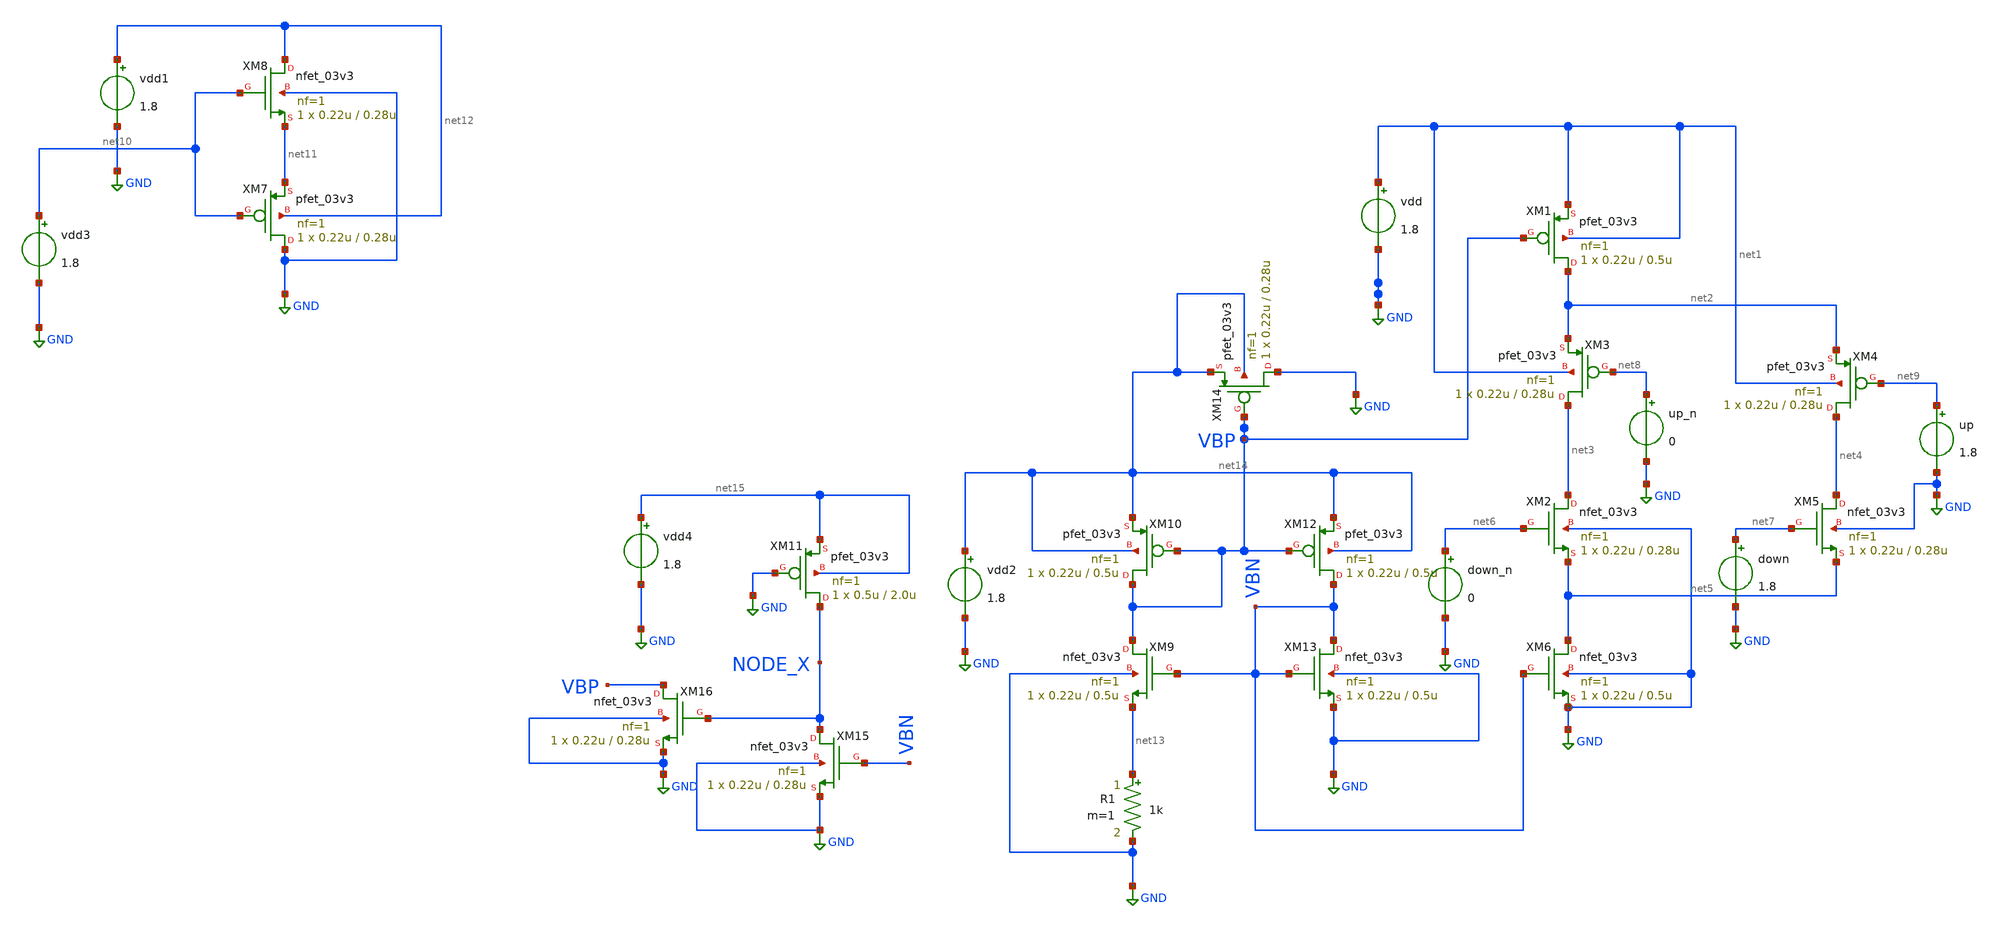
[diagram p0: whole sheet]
** sch_path: src/ChargePump/cp_amp.sch
* Copyright 2022 GlobalFoundries PDK Authors
* Licensed under the Apache License, Version 2.0 (the "License");
* you may not use this file except in compliance with the License.
* You may obtain a copy of the License at
* https://www.apache.org/licenses/LICENSE-2.0
* Unless required by applicable law or agreed to in writing, software
* distributed under the License is distributed on an "AS IS" BASIS,
* WITHOUT WARRANTIES OR CONDITIONS OF ANY KIND, either express or implied.
* See the License for the specific language governing permissions and
* limitations under the License.
**.subckt cp_amp
XM1 net2 VBP net1 net1 pfet_03v3 L=0.5u W=0.22u nf=1 ad='int((nf+1)/2) * W/nf * 0.18u' as='int((nf+2)/2) * W/nf * 0.18u'
+ pd='2*int((nf+1)/2) * (W/nf + 0.18u)' ps='2*int((nf+2)/2) * (W/nf + 0.18u)' nrd='0.18u / W' nrs='0.18u / W'
+ sa=0 sb=0 sd=0 m=1
XM2 net3 net6 net5 GND nfet_03v3 L=0.28u W=0.22u nf=1 ad='int((nf+1)/2) * W/nf * 0.18u' as='int((nf+2)/2) * W/nf * 0.18u'
+ pd='2*int((nf+1)/2) * (W/nf + 0.18u)' ps='2*int((nf+2)/2) * (W/nf + 0.18u)' nrd='0.18u / W' nrs='0.18u / W'
+ sa=0 sb=0 sd=0 m=1
vdd net1 GND 1.8
XM3 net3 net8 net2 net1 pfet_03v3 L=0.28u W=0.22u nf=1 ad='int((nf+1)/2) * W/nf * 0.18u' as='int((nf+2)/2) * W/nf * 0.18u'
+ pd='2*int((nf+1)/2) * (W/nf + 0.18u)' ps='2*int((nf+2)/2) * (W/nf + 0.18u)' nrd='0.18u / W' nrs='0.18u / W'
+ sa=0 sb=0 sd=0 m=1
XM4 net4 net9 net2 net1 pfet_03v3 L=0.28u W=0.22u nf=1 ad='int((nf+1)/2) * W/nf * 0.18u' as='int((nf+2)/2) * W/nf * 0.18u'
+ pd='2*int((nf+1)/2) * (W/nf + 0.18u)' ps='2*int((nf+2)/2) * (W/nf + 0.18u)' nrd='0.18u / W' nrs='0.18u / W'
+ sa=0 sb=0 sd=0 m=1
XM5 net4 net7 net5 GND nfet_03v3 L=0.28u W=0.22u nf=1 ad='int((nf+1)/2) * W/nf * 0.18u' as='int((nf+2)/2) * W/nf * 0.18u'
+ pd='2*int((nf+1)/2) * (W/nf + 0.18u)' ps='2*int((nf+2)/2) * (W/nf + 0.18u)' nrd='0.18u / W' nrs='0.18u / W'
+ sa=0 sb=0 sd=0 m=1
XM6 net5 VBN GND GND nfet_03v3 L=0.5u W=0.22u nf=1 ad='int((nf+1)/2) * W/nf * 0.18u' as='int((nf+2)/2) * W/nf * 0.18u'
+ pd='2*int((nf+1)/2) * (W/nf + 0.18u)' ps='2*int((nf+2)/2) * (W/nf + 0.18u)' nrd='0.18u / W' nrs='0.18u / W'
+ sa=0 sb=0 sd=0 m=1
down net7 GND 1.8
up net9 GND 1.8
up_n net8 GND 0
down_n net6 GND 0
XM7 GND net10 net11 net12 pfet_03v3 L=0.28u W=0.22u nf=1 ad='int((nf+1)/2) * W/nf * 0.18u' as='int((nf+2)/2) * W/nf * 0.18u'
+ pd='2*int((nf+1)/2) * (W/nf + 0.18u)' ps='2*int((nf+2)/2) * (W/nf + 0.18u)' nrd='0.18u / W' nrs='0.18u / W'
+ sa=0 sb=0 sd=0 m=1
XM8 net12 net10 net11 GND nfet_03v3 L=0.28u W=0.22u nf=1 ad='int((nf+1)/2) * W/nf * 0.18u' as='int((nf+2)/2) * W/nf * 0.18u'
+ pd='2*int((nf+1)/2) * (W/nf + 0.18u)' ps='2*int((nf+2)/2) * (W/nf + 0.18u)' nrd='0.18u / W' nrs='0.18u / W'
+ sa=0 sb=0 sd=0 m=1
vdd1 net12 GND 1.8
vdd2 net14 GND 1.8
XM10 VBP VBP net14 net14 pfet_03v3 L=0.5u W=0.22u nf=1 ad='int((nf+1)/2) * W/nf * 0.18u' as='int((nf+2)/2) * W/nf * 0.18u'
+ pd='2*int((nf+1)/2) * (W/nf + 0.18u)' ps='2*int((nf+2)/2) * (W/nf + 0.18u)' nrd='0.18u / W' nrs='0.18u / W'
+ sa=0 sb=0 sd=0 m=1
XM9 VBP VBN net13 GND nfet_03v3 L=0.5u W=0.22u nf=1 ad='int((nf+1)/2) * W/nf * 0.18u' as='int((nf+2)/2) * W/nf * 0.18u'
+ pd='2*int((nf+1)/2) * (W/nf + 0.18u)' ps='2*int((nf+2)/2) * (W/nf + 0.18u)' nrd='0.18u / W' nrs='0.18u / W'
+ sa=0 sb=0 sd=0 m=1
R1 net13 GND 1k m=1
XM12 VBN VBP net14 net14 pfet_03v3 L=0.5u W=0.22u nf=1 ad='int((nf+1)/2) * W/nf * 0.18u' as='int((nf+2)/2) * W/nf * 0.18u'
+ pd='2*int((nf+1)/2) * (W/nf + 0.18u)' ps='2*int((nf+2)/2) * (W/nf + 0.18u)' nrd='0.18u / W' nrs='0.18u / W'
+ sa=0 sb=0 sd=0 m=1
XM13 VBN VBN GND GND nfet_03v3 L=0.5u W=0.22u nf=1 ad='int((nf+1)/2) * W/nf * 0.18u' as='int((nf+2)/2) * W/nf * 0.18u'
+ pd='2*int((nf+1)/2) * (W/nf + 0.18u)' ps='2*int((nf+2)/2) * (W/nf + 0.18u)' nrd='0.18u / W' nrs='0.18u / W'
+ sa=0 sb=0 sd=0 m=1
XM14 GND VBP net14 net14 pfet_03v3 L=0.28u W=0.22u nf=1 ad='int((nf+1)/2) * W/nf * 0.18u' as='int((nf+2)/2) * W/nf * 0.18u'
+ pd='2*int((nf+1)/2) * (W/nf + 0.18u)' ps='2*int((nf+2)/2) * (W/nf + 0.18u)' nrd='0.18u / W' nrs='0.18u / W'
+ sa=0 sb=0 sd=0 m=1
vdd3 net10 GND 1.8
XM11 NODE_X GND net15 net15 pfet_03v3 L=2.0u W=0.5u nf=1 ad='int((nf+1)/2) * W/nf * 0.18u' as='int((nf+2)/2) * W/nf * 0.18u'
+ pd='2*int((nf+1)/2) * (W/nf + 0.18u)' ps='2*int((nf+2)/2) * (W/nf + 0.18u)' nrd='0.18u / W' nrs='0.18u / W'
+ sa=0 sb=0 sd=0 m=1
vdd4 net15 GND 1.8
XM15 NODE_X VBN GND GND nfet_03v3 L=0.28u W=0.22u nf=1 ad='int((nf+1)/2) * W/nf * 0.18u' as='int((nf+2)/2) * W/nf * 0.18u'
+ pd='2*int((nf+1)/2) * (W/nf + 0.18u)' ps='2*int((nf+2)/2) * (W/nf + 0.18u)' nrd='0.18u / W' nrs='0.18u / W'
+ sa=0 sb=0 sd=0 m=1
XM16 VBP NODE_X GND GND nfet_03v3 L=0.28u W=0.22u nf=1 ad='int((nf+1)/2) * W/nf * 0.18u' as='int((nf+2)/2) * W/nf * 0.18u'
+ pd='2*int((nf+1)/2) * (W/nf + 0.18u)' ps='2*int((nf+2)/2) * (W/nf + 0.18u)' nrd='0.18u / W' nrs='0.18u / W'
+ sa=0 sb=0 sd=0 m=1
**.ends
.GLOBAL GND
.end
